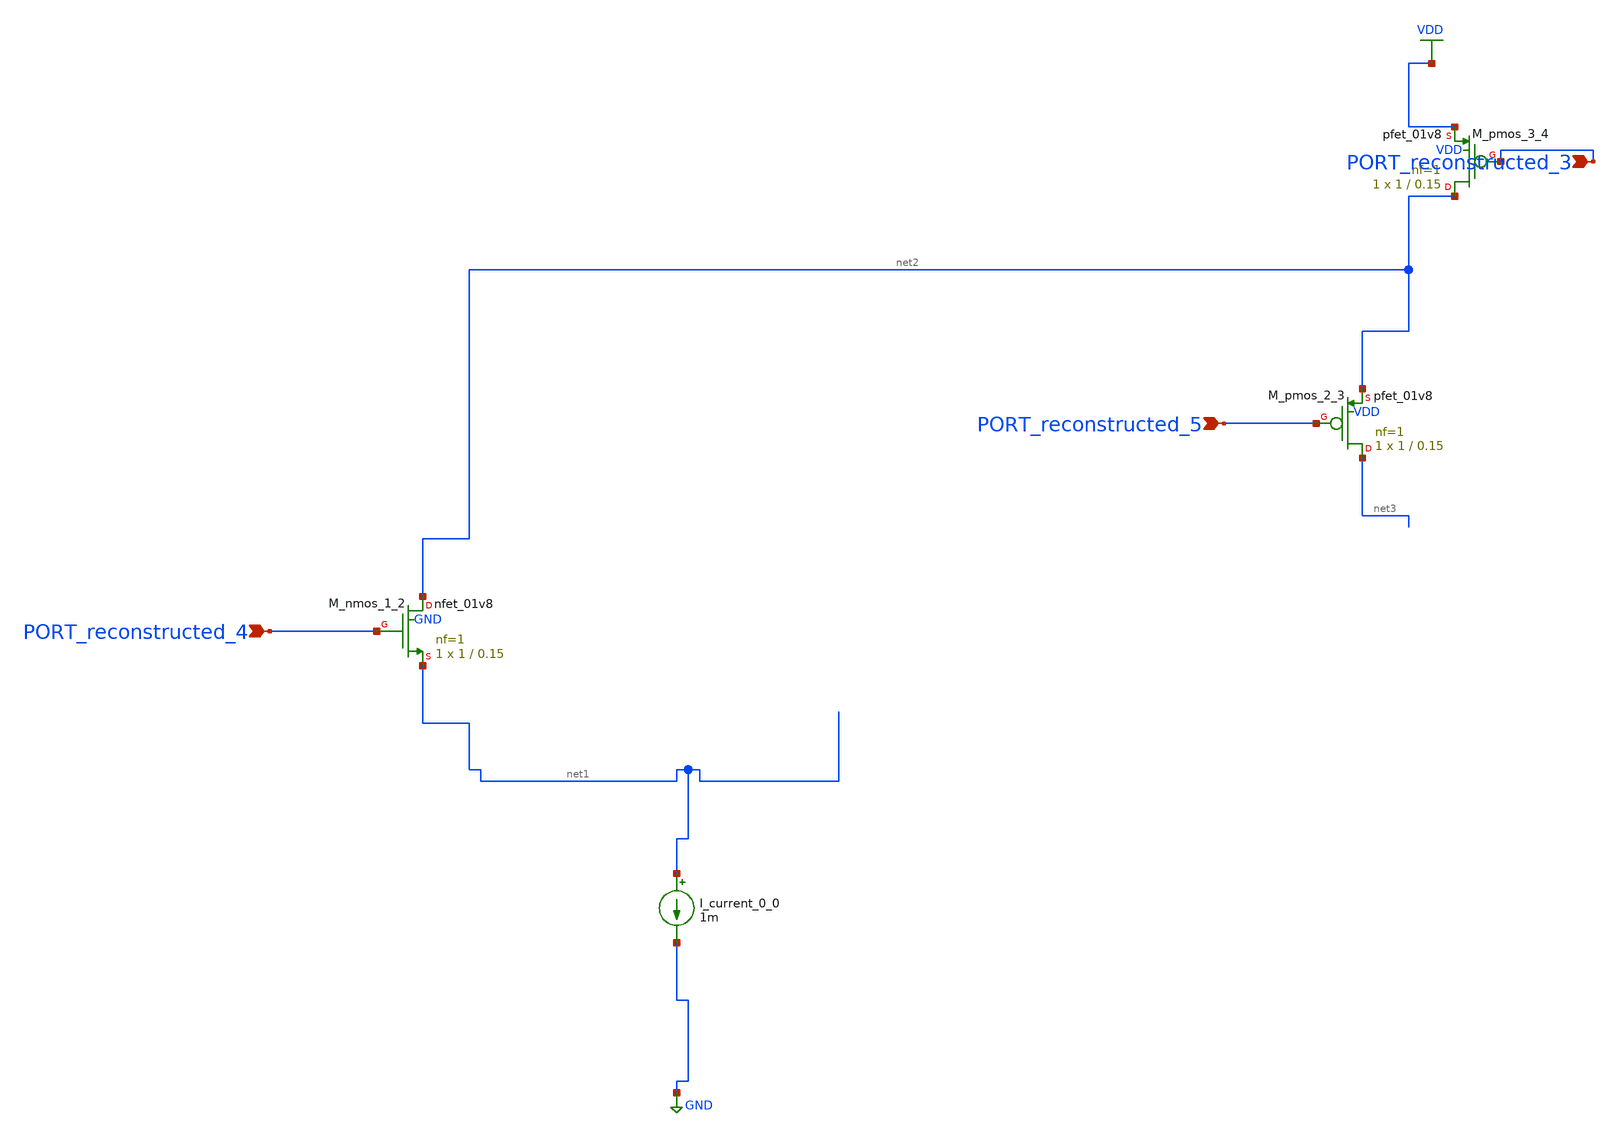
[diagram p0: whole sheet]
** sch_path: schematics/AMSNet/696.sch
**.subckt 696 PORT_reconstructed_4 PORT_reconstructed_5 PORT_reconstructed_3
*.ipin PORT_reconstructed_4
*.ipin PORT_reconstructed_5
*.ipin PORT_reconstructed_3
I_current_0_0 net1 GND 1m
XM_nmos_1_2 net2 PORT_reconstructed_4 net1 GND sky130_fd_pr__nfet_01v8 L=0.15 W=1 nf=1 ad='int((1 + 1)/2) * 1 / 1 * 0.29'
+ as='int((1 + 2)/2) * 1 / 1 * 0.29' pd='2*int((1 + 1)/2) * (1 / 1 + 0.29)' ps='2*int((1 + 2)/2) * (1 / 1 + 0.29)'
+ nrd='0.29 / 1 ' nrs='0.29 / 1 ' sa=0 sb=0 sd=0 mult=1 m=1
XM_pmos_2_3 net3 PORT_reconstructed_5 net2 VDD sky130_fd_pr__pfet_01v8 L=0.15 W=1 nf=1 ad='int((1 + 1)/2) * 1 / 1 * 0.29'
+ as='int((1 + 2)/2) * 1 / 1 * 0.29' pd='2*int((1 + 1)/2) * (1 / 1 + 0.29)' ps='2*int((1 + 2)/2) * (1 / 1 + 0.29)'
+ nrd='0.29 / 1 ' nrs='0.29 / 1 ' sa=0 sb=0 sd=0 mult=1 m=1
XM_pmos_3_4 net2 PORT_reconstructed_3 VDD VDD sky130_fd_pr__pfet_01v8 L=0.15 W=1 nf=1 ad='int((1 + 1)/2) * 1 / 1 * 0.29'
+ as='int((1 + 2)/2) * 1 / 1 * 0.29' pd='2*int((1 + 1)/2) * (1 / 1 + 0.29)' ps='2*int((1 + 2)/2) * (1 / 1 + 0.29)'
+ nrd='0.29 / 1 ' nrs='0.29 / 1 ' sa=0 sb=0 sd=0 mult=1 m=1
**.ends
.GLOBAL GND
.GLOBAL VDD
.end
